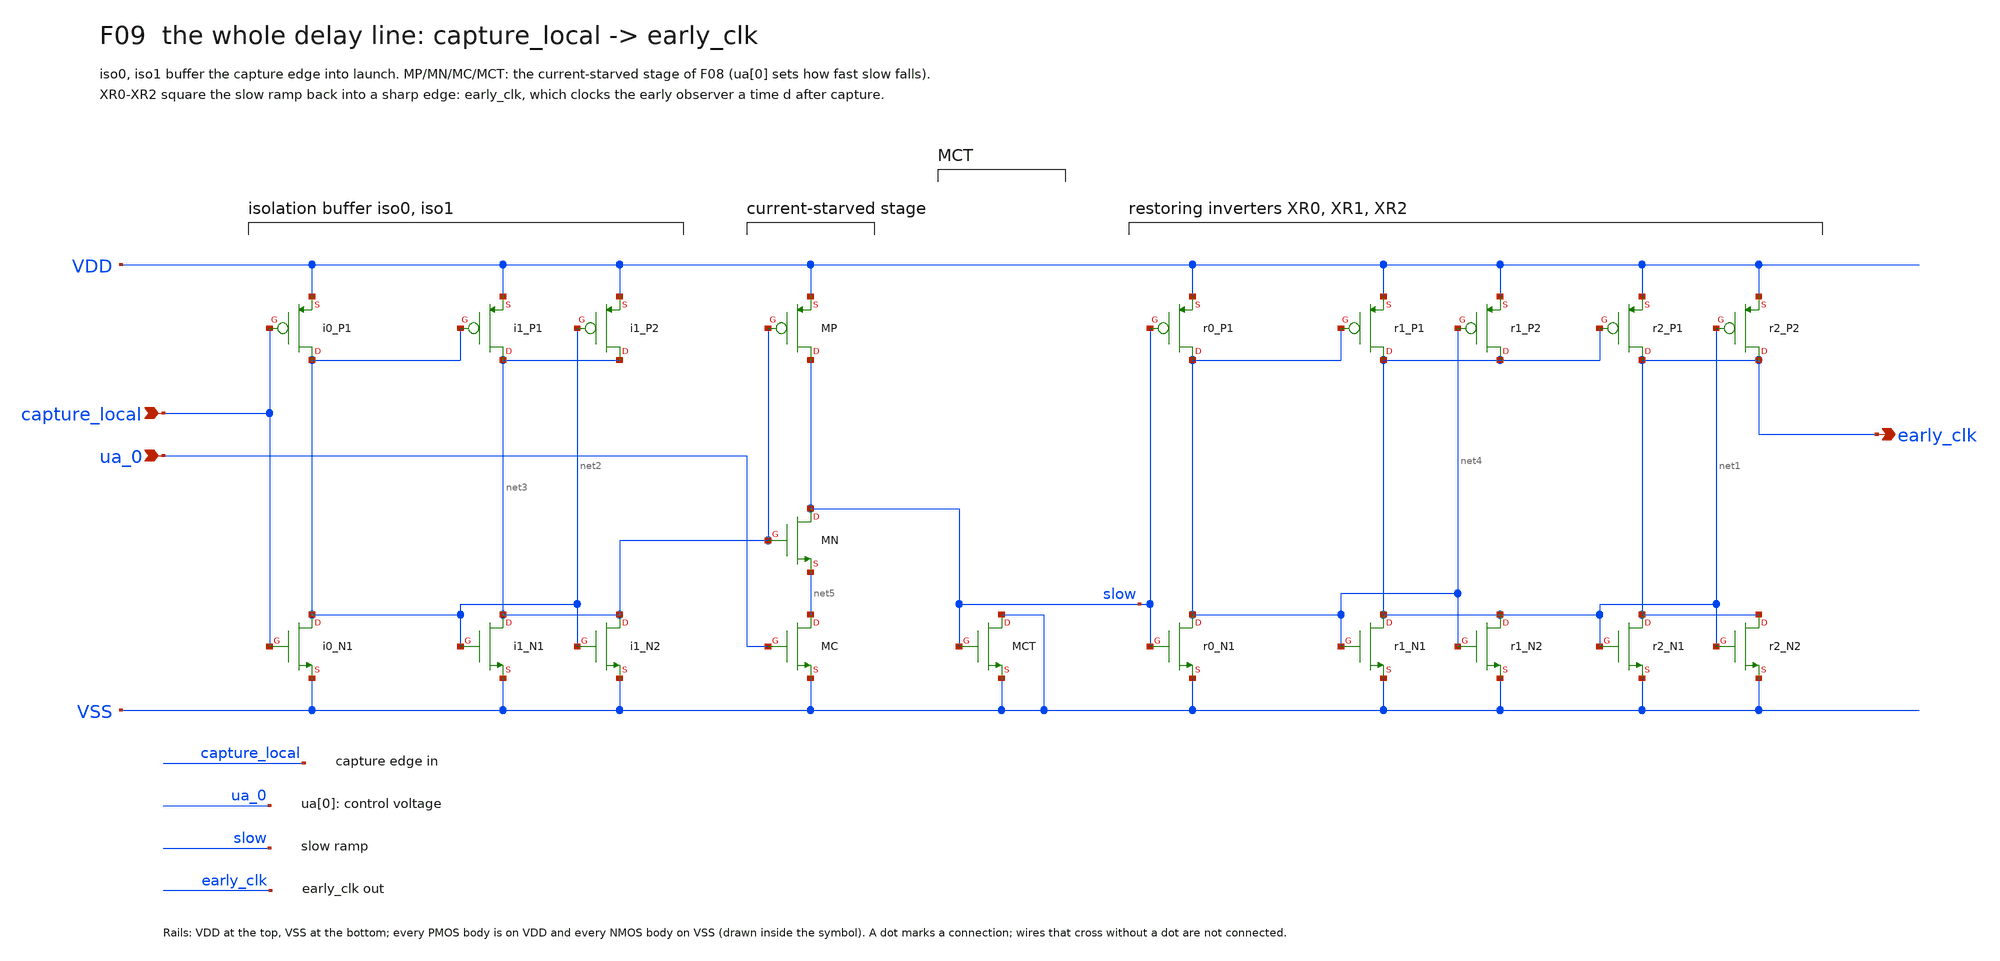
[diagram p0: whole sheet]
** sch_path: xschem/focus/F09_delay_line.sch
**.subckt F09_delay_line capture_local ua_0 early_clk
*.ipin capture_local
*.ipin ua_0
*.opin early_clk
Xi0_N1 net2 capture_local VSS VSS nfet_05v0 L=0.6u W=0.82u nf=1 m=1
Xi0_P1 net2 capture_local VDD VDD pfet_05v0 L=0.5u W=1.22u nf=1 m=1
Xi1_N1 net3 net2 VSS VSS nfet_05v0 L=0.6u W=0.82u nf=1 m=1
Xi1_N2 net3 net2 VSS VSS nfet_05v0 L=0.6u W=0.82u nf=1 m=1
Xi1_P1 net3 net2 VDD VDD pfet_05v0 L=0.5u W=1.22u nf=1 m=1
Xi1_P2 net3 net2 VDD VDD pfet_05v0 L=0.5u W=1.22u nf=1 m=1
Xr0_N1 net4 slow VSS VSS nfet_05v0 L=0.6u W=0.82u nf=1 m=1
Xr0_P1 net4 slow VDD VDD pfet_05v0 L=0.5u W=1.22u nf=1 m=1
Xr1_N1 net1 net4 VSS VSS nfet_05v0 L=0.6u W=0.82u nf=1 m=1
Xr1_N2 net1 net4 VSS VSS nfet_05v0 L=0.6u W=0.82u nf=1 m=1
Xr1_P1 net1 net4 VDD VDD pfet_05v0 L=0.5u W=1.22u nf=1 m=1
Xr1_P2 net1 net4 VDD VDD pfet_05v0 L=0.5u W=1.22u nf=1 m=1
Xr2_N1 early_clk net1 VSS VSS nfet_05v0 L=0.6u W=0.82u nf=1 m=1
Xr2_N2 early_clk net1 VSS VSS nfet_05v0 L=0.6u W=0.82u nf=1 m=1
Xr2_P1 early_clk net1 VDD VDD pfet_05v0 L=0.5u W=1.22u nf=1 m=1
Xr2_P2 early_clk net1 VDD VDD pfet_05v0 L=0.5u W=1.22u nf=1 m=1
XMP slow net3 VDD VDD pfet_05v0 L=0.5u W=1.22u nf=1 m=1
XMN slow net3 net5 VSS nfet_05v0 L=0.6u W=0.82u nf=1 m=1
XMC net5 ua_0 VSS VSS nfet_05v0 L=0.6u W=0.36u nf=1 m=1
XMCT VSS slow VSS VSS nfet_06v0 L=1u W=0.82u nf=1 m=1
**.ends
.end
